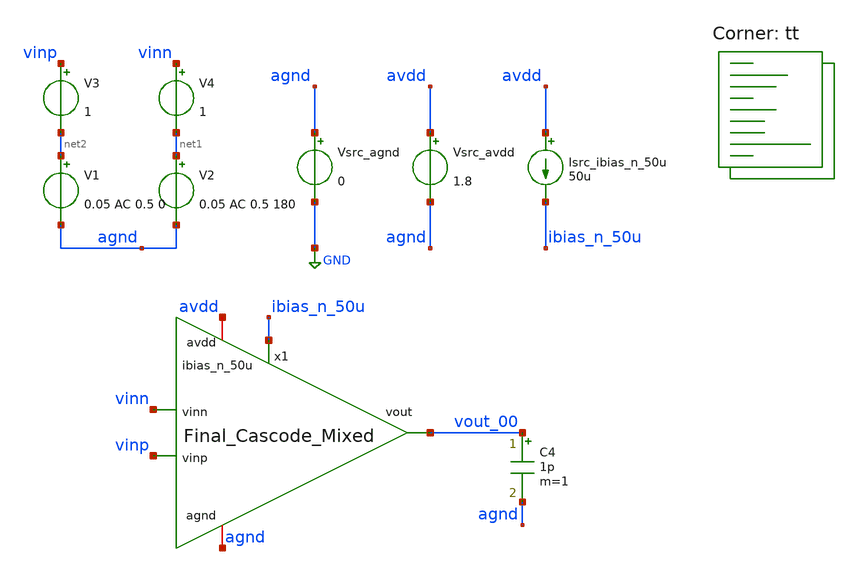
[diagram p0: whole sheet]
** sch_path: AMP/TB_Final_Cascode_Mixed.sch
**.subckt TB_Final_Cascode_Mixed
Vsrc_agnd agnd GND 0
Vsrc_avdd avdd agnd 1.8
Isrc_ibias_n_50u avdd ibias_n_50u 50u
C4 vout_00 agnd 1p m=1
V1 net2 agnd 0.05 AC 0.5 0
V2 net1 agnd 0.05 AC 0.5 180
x1 avdd vout_00 vinn vinp ibias_n_50u agnd Final_Cascode_Mixed
V3 vinp net2 1
V4 vinn net1 1
**** begin user architecture code

* this option enables mos model bin
* selection based on W/NF instead of W
.option wnflag=1

.option savecurrents

.control
save all
op

* Print newline
echo

set nmos_list = ( x1.xm1 x1.xm2 x1.xm9 x1.xm10 )
set pmos_list = ( x1.xm7 x1.xm8 )
set nmos_lvt_list = ( x1.xm3 x1.xm4 )
set pmos_lvt_list = ( x1.xm5 x1.xm6 )

* Print stats for each MOSFET
foreach nmos $nmos_list
 * Save stats
 save @m.{$nmos}.msky130_fd_pr__nfet_01v8[gm]
 let vth   = @m.{$nmos}.msky130_fd_pr__nfet_01v8[vth]
 let vgs   = @m.{$nmos}.msky130_fd_pr__nfet_01v8[vgs]
 let vds   = @m.{$nmos}.msky130_fd_pr__nfet_01v8[vds]
 let vdsat = @m.{$nmos}.msky130_fd_pr__nfet_01v8[vdsat]
 let gm    = @m.{$nmos}.msky130_fd_pr__nfet_01v8[gm]
 let gds   = @m.{$nmos}.msky130_fd_pr__nfet_01v8[gds]


 * Print stats
 echo Stats for $nmos:
 print vth
 print vgs
 print vds
 print vdsat
 print gm
 print gds

 * Print newline
 echo
end

foreach pmos $pmos_list
 * Save stats
 save @m.{$pmos}.msky130_fd_pr__nfet_01v8[gm]
 let vth   = @m.{$pmos}.msky130_fd_pr__pfet_01v8[vth]
 let vgs   = @m.{$pmos}.msky130_fd_pr__pfet_01v8[vgs]
 let vds   = @m.{$pmos}.msky130_fd_pr__pfet_01v8[vds]
 let vdsat = @m.{$pmos}.msky130_fd_pr__pfet_01v8[vdsat]
 let gm    = @m.{$pmos}.msky130_fd_pr__pfet_01v8[gm]
 let gds   = @m.{$pmos}.msky130_fd_pr__pfet_01v8[gds]

 * Print stats
 echo Stats for $pmos:
 print vth
 print vgs
 print vds
 print vdsat
 print gm
 print gds

 * Print newline
 echo
end

foreach nmos_lvt $nmos_lvt_list
 * Save stats
 save @m.{$nmos_lvt}.msky130_fd_pr__nfet_01v8_lvt[gm]
 let vth   = @m.{$nmos_lvt}.msky130_fd_pr__nfet_01v8_lvt[vth]
 let vgs   = @m.{$nmos_lvt}.msky130_fd_pr__nfet_01v8_lvt[vgs]
 let vds   = @m.{$nmos_lvt}.msky130_fd_pr__nfet_01v8_lvt[vds]
 let vdsat = @m.{$nmos_lvt}.msky130_fd_pr__nfet_01v8_lvt[vdsat]
 let gm    = @m.{$nmos_lvt}.msky130_fd_pr__nfet_01v8_lvt[gm]
 let gds   = @m.{$nmos_lvt}.msky130_fd_pr__nfet_01v8_lvt[gds]


 * Print stats
 echo Stats for $nmos_lvt:
 print vth
 print vgs
 print vds
 print vdsat
 print gm
 print gds

 * Print newline
 echo
end

foreach pmos_lvt $pmos_lvt_list
 * Save stats
 save @m.{$pmos_lvt}.msky130_fd_pr__nfet_01v8_lvt[gm]
 let vth   = @m.{$pmos_lvt}.msky130_fd_pr__pfet_01v8_lvt[vth]
 let vgs   = @m.{$pmos_lvt}.msky130_fd_pr__pfet_01v8_lvt[vgs]
 let vds   = @m.{$pmos_lvt}.msky130_fd_pr__pfet_01v8_lvt[vds]
 let vdsat = @m.{$pmos_lvt}.msky130_fd_pr__pfet_01v8_lvt[vdsat]
 let gm    = @m.{$pmos_lvt}.msky130_fd_pr__pfet_01v8_lvt[gm]
 let gds   = @m.{$pmos_lvt}.msky130_fd_pr__pfet_01v8_lvt[gds]


 * Print stats
 echo Stats for $pmos_lvt:
 print vth
 print vgs
 print vds
 print vdsat
 print gm
 print gds

 * Print newline
 echo
end

* Print region of operation
echo Regions of Operation:
echo

echo NMOS:
foreach nmos $nmos_list
 * Save stats
 let vds = @m.{$nmos}.msky130_fd_pr__nfet_01v8[vds]
 let vgs = @m.{$nmos}.msky130_fd_pr__nfet_01v8[vgs]
 let vth = @m.{$nmos}.msky130_fd_pr__nfet_01v8[vth]

 * Check and print regions
 if (vgs <= vth)
  echo $nmos: N Cutoff
  print vgs
  print vth
 end
 if (vgs > vth) & (vds <= (vgs - vth))
  echo $nmos: N Triode
  print vgs
  print vth
  print vds
 end
 if (vgs > vth) & (vds > (vgs - vth))
  echo $nmos: N Saturation
 end
end
echo

echo PMOS:
foreach pmos $pmos_list
 * Save stats
 let vds = @m.{$pmos}.msky130_fd_pr__pfet_01v8[vds]
 let vgs = @m.{$pmos}.msky130_fd_pr__pfet_01v8[vgs]
 let vth = @m.{$pmos}.msky130_fd_pr__pfet_01v8[vth]

 * Check and print regions
 if (abs(vgs) <= abs(vth))
  echo $pmos: P Cutoff
  print vgs
  print vth
 end
 if (abs(vgs) > abs(vth)) & (abs(vds) <= (abs(vgs) - abs(vth)))
  echo $pmos: P Triode
  print vgs
  print vth
  print vds
 end
 if (abs(vgs) > abs(vth)) & (abs(vds) > (abs(vgs) - abs(vth)))
  echo $pmos: P Saturation
 end
end
echo

echo NMOS_lvt:
foreach nmos_lvt $nmos_lvt_list
 * Save stats
 let vds = @m.{$nmos_lvt}.msky130_fd_pr__nfet_01v8_lvt[vds]
 let vgs = @m.{$nmos_lvt}.msky130_fd_pr__nfet_01v8_lvt[vgs]
 let vth = @m.{$nmos_lvt}.msky130_fd_pr__nfet_01v8_lvt[vth]

 * Check and print regions
 if (vgs <= vth)
  echo $nmos_lvt: N Cutoff
  print vgs
  print vth
 end
 if (vgs > vth) & (vds <= (vgs - vth))
  echo $nmos_lvt: N Triode
  print vgs
  print vth
  print vds
 end
 if (vgs > vth) & (vds > (vgs - vth))
  echo $nmos_lvt: N Saturation
 end
end
echo

echo PMOS_lvt:
foreach pmos_lvt $pmos_lvt_list
 * Save stats
 let vds = @m.{$pmos_lvt}.msky130_fd_pr__pfet_01v8_lvt[vds]
 let vgs = @m.{$pmos_lvt}.msky130_fd_pr__pfet_01v8_lvt[vgs]
 let vth = @m.{$pmos_lvt}.msky130_fd_pr__pfet_01v8_lvt[vth]

 * Check and print regions
 if (abs(vgs) <= abs(vth))
  echo $pmos_lvt: P Cutoff
  print vgs
  print vth
 end
 if (abs(vgs) > abs(vth)) & (abs(vds) <= (abs(vgs) - abs(vth)))
  echo $pmos_lvt: P Triode
  print vgs
  print vth
  print vds
 end
 if (abs(vgs) > abs(vth)) & (abs(vds) > (abs(vgs) - abs(vth)))
  echo $pmos_lvt: P Saturation
 end
end
echo

* Sweep frequency
write TB_Final_Cascode_Mixed.raw
set appendwrite
ac dec 100 1 1e11
remzerovec

* Calculate gain
let vin_diff = v(vinp) - v(vinn)

let vout_00 = v(vout_00)
let gain_sch = db(mag(vout_00/vin_diff))
let ratio_sch = (vout_00/vin_diff)

*let vout_01 = v(vout_01)
*let gain_gds = db(mag(vout_01/vin_diff))
*let ratio_gds = (vout_01/vin_diff)

write TB_Final_Cascode_Mixed.raw

.endc


.lib $::SKYWATER_MODELS/sky130.lib.spice tt
**** end user architecture code
**.ends

* expanding   symbol:
*+  /foss/designs/EE437/Project/ee437-quantum-controller/AMP/Final_Cascode_Mixed.sym # of pins=6
** sym_path: AMP/Final_Cascode_Mixed.sym
** sch_path: AMP/Final_Cascode_Mixed.sch
.subckt Final_Cascode_Mixed avdd vout vinn vinp ibias_n_50u agnd
*.iopin avdd
*.ipin vinp
*.opin vout
*.iopin agnd
*.ipin vinn
*.ipin ibias_n_50u
XM1 int_n1 vinp_cm itail agnd sky130_fd_pr__nfet_01v8 L=0.15 W=4.00 nf=4 ad='int((nf+1)/2) * W/nf * 0.29'
+ as='int((nf+2)/2) * W/nf * 0.29' pd='2*int((nf+1)/2) * (W/nf + 0.29)' ps='2*int((nf+2)/2) * (W/nf + 0.29)'
+ nrd='0.29 / W' nrs='0.29 / W' sa=0 sb=0 sd=0 mult=1 m=1
XM2 int_n2 vinn_cm itail agnd sky130_fd_pr__nfet_01v8 L=0.15 W=4.00 nf=4 ad='int((nf+1)/2) * W/nf * 0.29'
+ as='int((nf+2)/2) * W/nf * 0.29' pd='2*int((nf+1)/2) * (W/nf + 0.29)' ps='2*int((nf+2)/2) * (W/nf + 0.29)'
+ nrd='0.29 / W' nrs='0.29 / W' sa=0 sb=0 sd=0 mult=1 m=1
XM7 int_p1 Vb3 avdd avdd sky130_fd_pr__pfet_01v8 L=0.15 W=10.00 nf=4 ad='int((nf+1)/2) * W/nf * 0.29'
+ as='int((nf+2)/2) * W/nf * 0.29' pd='2*int((nf+1)/2) * (W/nf + 0.29)' ps='2*int((nf+2)/2) * (W/nf + 0.29)'
+ nrd='0.29 / W' nrs='0.29 / W' sa=0 sb=0 sd=0 mult=1 m=1
XM8 int_p2 Vb3 avdd avdd sky130_fd_pr__pfet_01v8 L=0.15 W=10.00 nf=4 ad='int((nf+1)/2) * W/nf * 0.29'
+ as='int((nf+2)/2) * W/nf * 0.29' pd='2*int((nf+1)/2) * (W/nf + 0.29)' ps='2*int((nf+2)/2) * (W/nf + 0.29)'
+ nrd='0.29 / W' nrs='0.29 / W' sa=0 sb=0 sd=0 mult=1 m=1
XM9 ibias_n_50u ibias_n_50u agnd agnd sky130_fd_pr__nfet_01v8 L=0.15 W=4.00 nf=1 ad='int((nf+1)/2) * W/nf * 0.29'
+ as='int((nf+2)/2) * W/nf * 0.29' pd='2*int((nf+1)/2) * (W/nf + 0.29)' ps='2*int((nf+2)/2) * (W/nf + 0.29)'
+ nrd='0.29 / W' nrs='0.29 / W' sa=0 sb=0 sd=0 mult=2 m=2
XM10 itail ibias_n_50u agnd agnd sky130_fd_pr__nfet_01v8 L=0.15 W=32.00 nf=1 ad='int((nf+1)/2) * W/nf * 0.29'
+ as='int((nf+2)/2) * W/nf * 0.29' pd='2*int((nf+1)/2) * (W/nf + 0.29)' ps='2*int((nf+2)/2) * (W/nf + 0.29)'
+ nrd='0.29 / W' nrs='0.29 / W' sa=0 sb=0 sd=0 mult=2 m=2
XM3 Vb3 Vb1 int_n1 agnd sky130_fd_pr__nfet_01v8_lvt L=0.15 W=12.00 nf=4 ad='int((nf+1)/2) * W/nf * 0.29'
+ as='int((nf+2)/2) * W/nf * 0.29' pd='2*int((nf+1)/2) * (W/nf + 0.29)' ps='2*int((nf+2)/2) * (W/nf + 0.29)'
+ nrd='0.29 / W' nrs='0.29 / W' sa=0 sb=0 sd=0 mult=1 m=1
XM4 vout_int Vb1 int_n2 agnd sky130_fd_pr__nfet_01v8_lvt L=0.15 W=12.00 nf=4 ad='int((nf+1)/2) * W/nf * 0.29'
+ as='int((nf+2)/2) * W/nf * 0.29' pd='2*int((nf+1)/2) * (W/nf + 0.29)' ps='2*int((nf+2)/2) * (W/nf + 0.29)'
+ nrd='0.29 / W' nrs='0.29 / W' sa=0 sb=0 sd=0 mult=1 m=1
XM5 Vb3 Vb2 int_p1 avdd sky130_fd_pr__pfet_01v8_lvt L=0.35 W=32.00 nf=4 ad='int((nf+1)/2) * W/nf * 0.29'
+ as='int((nf+2)/2) * W/nf * 0.29' pd='2*int((nf+1)/2) * (W/nf + 0.29)' ps='2*int((nf+2)/2) * (W/nf + 0.29)'
+ nrd='0.29 / W' nrs='0.29 / W' sa=0 sb=0 sd=0 mult=1 m=1
XM6 vout_int Vb2 int_p2 avdd sky130_fd_pr__pfet_01v8_lvt L=0.35 W=32.00 nf=4 ad='int((nf+1)/2) * W/nf * 0.29'
+ as='int((nf+2)/2) * W/nf * 0.29' pd='2*int((nf+1)/2) * (W/nf + 0.29)' ps='2*int((nf+2)/2) * (W/nf + 0.29)'
+ nrd='0.29 / W' nrs='0.29 / W' sa=0 sb=0 sd=0 mult=1 m=1
XM11 tail ibias_n_50u agnd agnd sky130_fd_pr__nfet_01v8 L=0.15 W=8 nf=1 ad='int((nf+1)/2) * W/nf * 0.29'
+ as='int((nf+2)/2) * W/nf * 0.29' pd='2*int((nf+1)/2) * (W/nf + 0.29)' ps='2*int((nf+2)/2) * (W/nf + 0.29)'
+ nrd='0.29 / W' nrs='0.29 / W' sa=0 sb=0 sd=0 mult=1 m=1
XM12 vcm_d vcm_d tail agnd sky130_fd_pr__nfet_01v8 L=0.15 W=0.5 nf=1 ad='int((nf+1)/2) * W/nf * 0.29'
+ as='int((nf+2)/2) * W/nf * 0.29' pd='2*int((nf+1)/2) * (W/nf + 0.29)' ps='2*int((nf+2)/2) * (W/nf + 0.29)'
+ nrd='0.29 / W' nrs='0.29 / W' sa=0 sb=0 sd=0 mult=1 m=1
XM13 vcm_d vcm_d avdd avdd sky130_fd_pr__pfet_01v8_lvt L=0.35 W=20 nf=1 ad='int((nf+1)/2) * W/nf * 0.29'
+ as='int((nf+2)/2) * W/nf * 0.29' pd='2*int((nf+1)/2) * (W/nf + 0.29)' ps='2*int((nf+2)/2) * (W/nf + 0.29)'
+ nrd='0.29 / W' nrs='0.29 / W' sa=0 sb=0 sd=0 mult=1 m=1
XM14 vcm_d avdd vinn_cm agnd sky130_fd_pr__nfet_01v8_lvt L=2 W=0.5 nf=1 ad='int((nf+1)/2) * W/nf * 0.29'
+ as='int((nf+2)/2) * W/nf * 0.29' pd='2*int((nf+1)/2) * (W/nf + 0.29)' ps='2*int((nf+2)/2) * (W/nf + 0.29)'
+ nrd='0.29 / W' nrs='0.29 / W' sa=0 sb=0 sd=0 mult=1 m=1
XM15 vcm_d avdd vinp_cm agnd sky130_fd_pr__nfet_01v8_lvt L=2 W=0.5 nf=1 ad='int((nf+1)/2) * W/nf * 0.29'
+ as='int((nf+2)/2) * W/nf * 0.29' pd='2*int((nf+1)/2) * (W/nf + 0.29)' ps='2*int((nf+2)/2) * (W/nf + 0.29)'
+ nrd='0.29 / W' nrs='0.29 / W' sa=0 sb=0 sd=0 mult=1 m=1
XC3 vinp_cm vinp sky130_fd_pr__cap_mim_m3_1 W=100 L=100 MF=1 m=1
XC1 vinn_cm vinn sky130_fd_pr__cap_mim_m3_1 W=100 L=100 MF=1 m=1
XM16 Vb2 ibias_n_50u agnd agnd sky130_fd_pr__nfet_01v8 L=0.5 W=12 nf=4 ad='int((nf+1)/2) * W/nf * 0.29'
+ as='int((nf+2)/2) * W/nf * 0.29' pd='2*int((nf+1)/2) * (W/nf + 0.29)' ps='2*int((nf+2)/2) * (W/nf + 0.29)'
+ nrd='0.29 / W' nrs='0.29 / W' sa=0 sb=0 sd=0 mult=1 m=1
XM17 avdd avdd Vb2 agnd sky130_fd_pr__nfet_01v8_lvt L=0.15 W=2 nf=1 ad='int((nf+1)/2) * W/nf * 0.29'
+ as='int((nf+2)/2) * W/nf * 0.29' pd='2*int((nf+1)/2) * (W/nf + 0.29)' ps='2*int((nf+2)/2) * (W/nf + 0.29)'
+ nrd='0.29 / W' nrs='0.29 / W' sa=0 sb=0 sd=0 mult=1 m=1
XM19 Vb1 Vb1 avdd avdd sky130_fd_pr__pfet_01v8_lvt L=0.35 W=1 nf=1 ad='int((nf+1)/2) * W/nf * 0.29' as='int((nf+2)/2) * W/nf * 0.29'
+ pd='2*int((nf+1)/2) * (W/nf + 0.29)' ps='2*int((nf+2)/2) * (W/nf + 0.29)' nrd='0.29 / W' nrs='0.29 / W'
+ sa=0 sb=0 sd=0 mult=32 m=32
XM18 Vb1 Vb1 agnd agnd sky130_fd_pr__nfet_01v8 L=0.8 W=0.5 nf=1 ad='int((nf+1)/2) * W/nf * 0.29' as='int((nf+2)/2) * W/nf * 0.29'
+ pd='2*int((nf+1)/2) * (W/nf + 0.29)' ps='2*int((nf+2)/2) * (W/nf + 0.29)' nrd='0.29 / W' nrs='0.29 / W'
+ sa=0 sb=0 sd=0 mult=1 m=1
XM20 vout vout_int agnd agnd sky130_fd_pr__nfet_01v8 L=0.15 W=20 nf=10 ad='int((nf+1)/2) * W/nf * 0.29'
+ as='int((nf+2)/2) * W/nf * 0.29' pd='2*int((nf+1)/2) * (W/nf + 0.29)' ps='2*int((nf+2)/2) * (W/nf + 0.29)'
+ nrd='0.29 / W' nrs='0.29 / W' sa=0 sb=0 sd=0 mult=1 m=1
XM21 avdd avdd vout agnd sky130_fd_pr__nfet_01v8 L=0.15 W=10 nf=10 ad='int((nf+1)/2) * W/nf * 0.29' as='int((nf+2)/2) * W/nf * 0.29'
+ pd='2*int((nf+1)/2) * (W/nf + 0.29)' ps='2*int((nf+2)/2) * (W/nf + 0.29)' nrd='0.29 / W' nrs='0.29 / W'
+ sa=0 sb=0 sd=0 mult=1 m=1
.ends

.GLOBAL GND
.end
